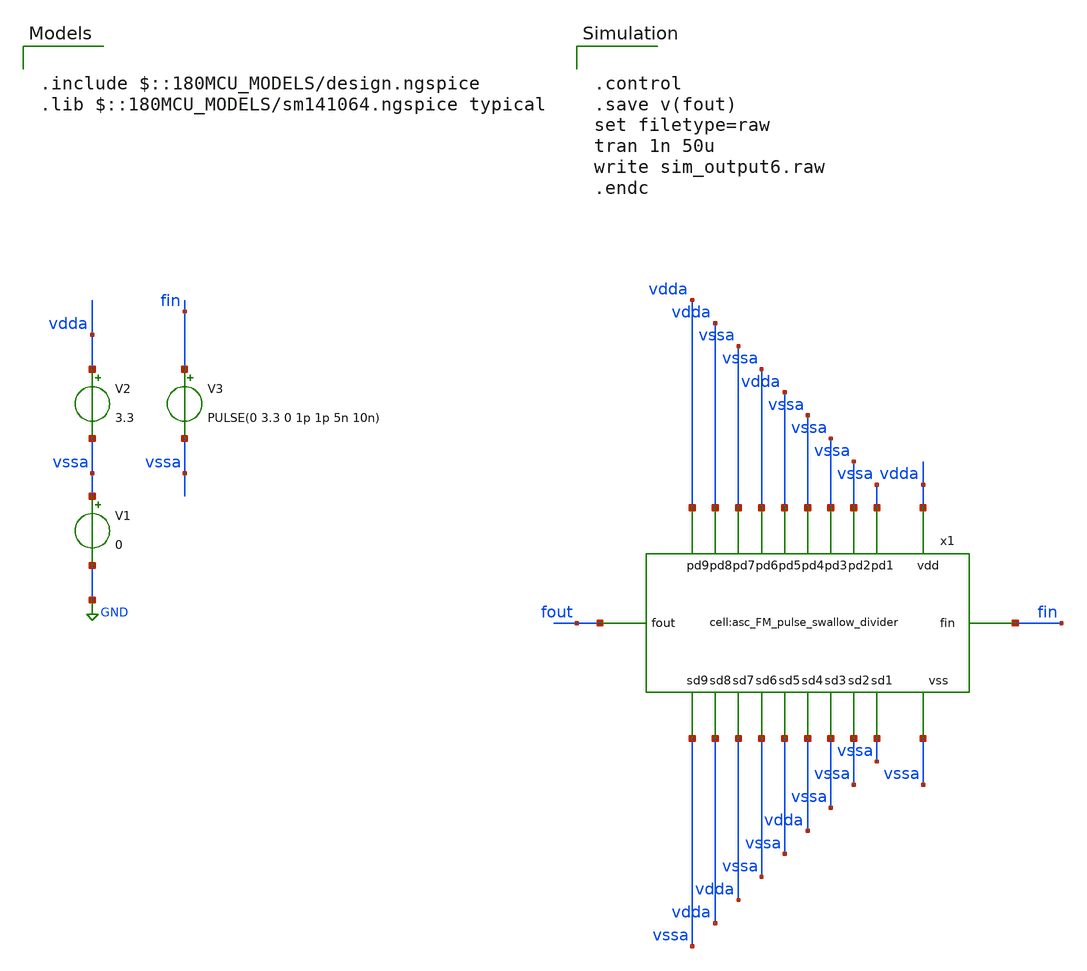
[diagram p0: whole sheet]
** sch_path: designs/libs/xp_tb_analog/tb_asc_FM_pulse_swallow_divider/tb_asc_FM_pulse_swallow_divider.sch
**.subckt tb_asc_FM_pulse_swallow_divider
V1 vssa GND 0
V2 vdda vssa 3.3
V3 fin vssa PULSE(0 3.3 0 1p 1p 5n 10n)
x1 fout vssa vdda vdda vssa vssa vdda vssa vssa vssa vssa fin vdda vdda vdda vssa vssa vdda vssa
+ vssa vssa vssa asc_FM_pulse_swallow_divider
**** begin user architecture code

.include $::180MCU_MODELS/design.ngspice
.lib $::180MCU_MODELS/sm141064.ngspice typical



.control
.save v(fout)
set filetype=raw
tran 1n 50u
write sim_output6.raw
.endc


**** end user architecture code
**.ends
.GLOBAL GND
.end
